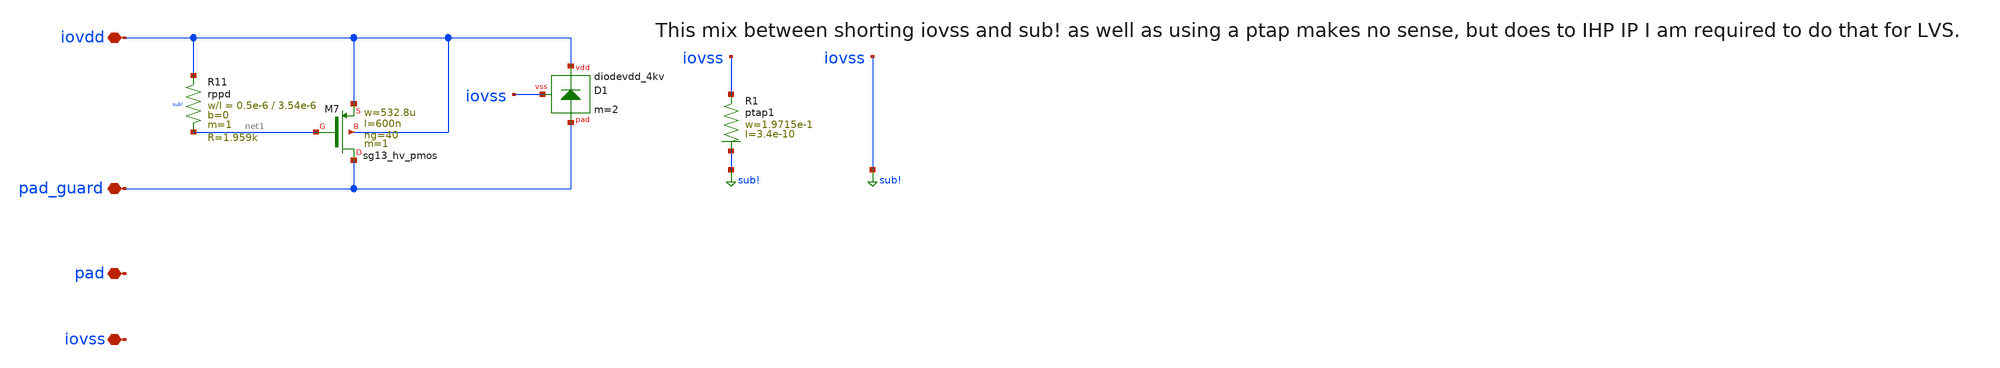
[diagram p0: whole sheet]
** sch_path: trident_test_structures/design_data/xschem/IOPadAnalogGuardLayer/guard_vdd_first_stage_esd.sch
**.subckt guard_vdd_first_stage_esd iovss pad_guard iovdd pad
*.iopin iovss
*.iopin pad_guard
*.iopin iovdd
*.iopin pad
XM7 pad_guard net1 iovdd iovdd sg13_hv_pmos w=532.8u l=600n ng=40 m=1 mm_ok=1
XR11 iovdd net1 sub! rppd w=0.5e-6 l=3.54e-6 m=1 b=0 mm_ok=1
XD1 iovdd pad_guard iovss diodevdd_4kv m=2
XR1 iovss sub! ptap1 R=2.485m w=1.9715e-1 l=3.4e-10
**.ends
.GLOBAL sub!
.end
